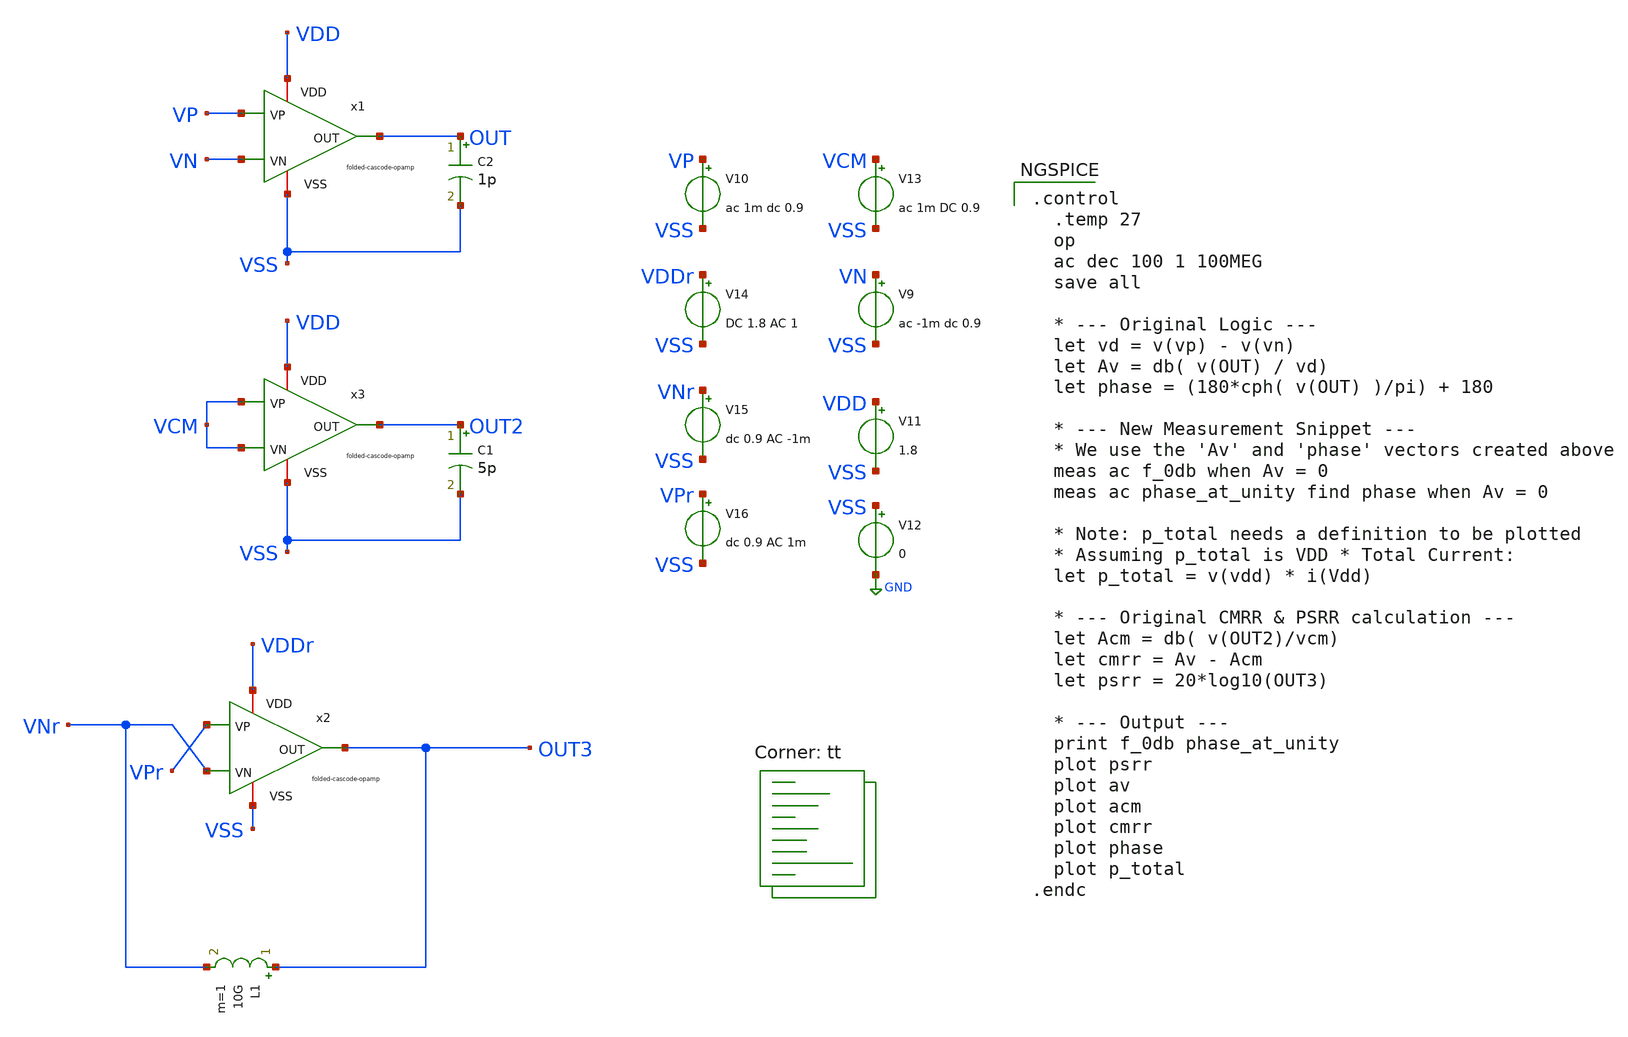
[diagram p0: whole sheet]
** sch_path: bandgap/bgr-opamp2/tb_ac.sch
**.subckt tb_ac
C2 OUT VSS 1p m=1
C1 OUT2 VSS 5p m=1
L1 OUT3 VNr 10G m=1
V9 VN VSS ac -1m dc 0.9
V10 VP VSS ac 1m dc 0.9
V11 VDD VSS 1.8
V12 VSS GND 0
V13 VCM VSS ac 1m DC 0.9
V14 VDDr VSS DC 1.8 AC 1
V15 VNr VSS dc 0.9 AC -1m
V16 VPr VSS dc 0.9 AC 1m
x1 OUT VDD VP VN VSS folded-cascode-opamp
x2 OUT3 VDDr VPr VNr VSS folded-cascode-opamp
x3 OUT2 VDD VCM VCM VSS folded-cascode-opamp
**** begin user architecture code

.control
  .temp 27
  op
  ac dec 100 1 100MEG
  save all

  * --- Original Logic ---
  let vd = v(vp) - v(vn)
  let Av = db( v(OUT) / vd)
  let phase = (180*cph( v(OUT) )/pi) + 180

  * --- New Measurement Snippet ---
  * We use the 'Av' and 'phase' vectors created above
  meas ac f_0db when Av = 0
  meas ac phase_at_unity find phase when Av = 0

  * Note: p_total needs a definition to be plotted
  * Assuming p_total is VDD * Total Current:
  let p_total = v(vdd) * i(Vdd)

  * --- Original CMRR & PSRR calculation ---
  let Acm = db( v(OUT2)/vcm)
  let cmrr = Av - Acm
  let psrr = 20*log10(OUT3)

  * --- Output ---
  print f_0db phase_at_unity
  plot psrr
  plot av
  plot acm
  plot cmrr
  plot phase
  plot p_total
.endc



.lib $::SKYWATER_MODELS/sky130.lib.spice tt
**** end user architecture code
**.ends

* expanding   symbol:  afe-icdec-teknofest-2026/bandgap/bgr-opamp2/folded-cascode-opamp.sym # of
*+ pins=5
** sym_path: bandgap/bgr-opamp2/folded-cascode-opamp.sym
** sch_path: bandgap/bgr-opamp2/folded-cascode-opamp.sch
.subckt folded-cascode-opamp OUT VDD VP VN VSS
*.iopin VSS
*.iopin VDD
*.ipin VP
*.ipin VN
*.opin OUT
XR10 VSS net8 VSS sky130_fd_pr__res_high_po_1p41 L=1.235 mult=1 m=1
XM19 net2 net2 VSS GND sky130_fd_pr__nfet_01v8_lvt L=0.5 W=6.4 nf=1 ad='int((nf+1)/2) * W/nf * 0.29'
+ as='int((nf+2)/2) * W/nf * 0.29' pd='2*int((nf+1)/2) * (W/nf + 0.29)' ps='2*int((nf+2)/2) * (W/nf + 0.29)'
+ nrd='0.29 / W' nrs='0.29 / W' sa=0 sb=0 sd=0 mult=1 m=1
XM20 net3 net2 net9 GND sky130_fd_pr__nfet_01v8_lvt L=0.5 W=6.4 nf=1 ad='int((nf+1)/2) * W/nf * 0.29'
+ as='int((nf+2)/2) * W/nf * 0.29' pd='2*int((nf+1)/2) * (W/nf + 0.29)' ps='2*int((nf+2)/2) * (W/nf + 0.29)'
+ nrd='0.29 / W' nrs='0.29 / W' sa=0 sb=0 sd=0 mult=1 m=1
XM16 net4 net1 VDD VDD sky130_fd_pr__pfet_01v8_lvt L=0.5 W=20.8 nf=1 ad='int((nf+1)/2) * W/nf * 0.29'
+ as='int((nf+2)/2) * W/nf * 0.29' pd='2*int((nf+1)/2) * (W/nf + 0.29)' ps='2*int((nf+2)/2) * (W/nf + 0.29)'
+ nrd='0.29 / W' nrs='0.29 / W' sa=0 sb=0 sd=0 mult=1 m=1
XM13 net1 net1 VDD VDD sky130_fd_pr__pfet_01v8_lvt L=0.5 W=20.8 nf=1 ad='int((nf+1)/2) * W/nf * 0.29'
+ as='int((nf+2)/2) * W/nf * 0.29' pd='2*int((nf+1)/2) * (W/nf + 0.29)' ps='2*int((nf+2)/2) * (W/nf + 0.29)'
+ nrd='0.29 / W' nrs='0.29 / W' sa=0 sb=0 sd=0 mult=1 m=1
XM14 net2 net3 net4 VDD sky130_fd_pr__pfet_01v8_lvt L=0.5 W=20.8 nf=1 ad='int((nf+1)/2) * W/nf * 0.29'
+ as='int((nf+2)/2) * W/nf * 0.29' pd='2*int((nf+1)/2) * (W/nf + 0.29)' ps='2*int((nf+2)/2) * (W/nf + 0.29)'
+ nrd='0.29 / W' nrs='0.29 / W' sa=0 sb=0 sd=0 mult=1 m=1
XM17 net3 net3 net1 VDD sky130_fd_pr__pfet_01v8_lvt L=0.5 W=20.8 nf=1 ad='int((nf+1)/2) * W/nf * 0.29'
+ as='int((nf+2)/2) * W/nf * 0.29' pd='2*int((nf+1)/2) * (W/nf + 0.29)' ps='2*int((nf+2)/2) * (W/nf + 0.29)'
+ nrd='0.29 / W' nrs='0.29 / W' sa=0 sb=0 sd=0 mult=1 m=1
XM18 net10 net1 VDD VDD sky130_fd_pr__pfet_01v8_lvt L=0.5 W=20.8 nf=1 ad='int((nf+1)/2) * W/nf * 0.29'
+ as='int((nf+2)/2) * W/nf * 0.29' pd='2*int((nf+1)/2) * (W/nf + 0.29)' ps='2*int((nf+2)/2) * (W/nf + 0.29)'
+ nrd='0.29 / W' nrs='0.29 / W' sa=0 sb=0 sd=0 mult=1 m=1
XM21 net11 net3 net10 VDD sky130_fd_pr__pfet_01v8_lvt L=0.5 W=20.8 nf=1 ad='int((nf+1)/2) * W/nf * 0.29'
+ as='int((nf+2)/2) * W/nf * 0.29' pd='2*int((nf+1)/2) * (W/nf + 0.29)' ps='2*int((nf+2)/2) * (W/nf + 0.29)'
+ nrd='0.29 / W' nrs='0.29 / W' sa=0 sb=0 sd=0 mult=1 m=1
XM22 net11 net11 net13 GND sky130_fd_pr__nfet_01v8_lvt L=0.5 W=1.45 nf=1 ad='int((nf+1)/2) * W/nf * 0.29'
+ as='int((nf+2)/2) * W/nf * 0.29' pd='2*int((nf+1)/2) * (W/nf + 0.29)' ps='2*int((nf+2)/2) * (W/nf + 0.29)'
+ nrd='0.29 / W' nrs='0.29 / W' sa=0 sb=0 sd=0 mult=1 m=1
XM23 net13 net11 net12 GND sky130_fd_pr__nfet_01v8_lvt L=0.5 W=1.45 nf=1 ad='int((nf+1)/2) * W/nf * 0.29'
+ as='int((nf+2)/2) * W/nf * 0.29' pd='2*int((nf+1)/2) * (W/nf + 0.29)' ps='2*int((nf+2)/2) * (W/nf + 0.29)'
+ nrd='0.29 / W' nrs='0.29 / W' sa=0 sb=0 sd=0 mult=1 m=1
XM24 net12 net11 VSS GND sky130_fd_pr__nfet_01v8_lvt L=0.5 W=1.45 nf=1 ad='int((nf+1)/2) * W/nf * 0.29'
+ as='int((nf+2)/2) * W/nf * 0.29' pd='2*int((nf+1)/2) * (W/nf + 0.29)' ps='2*int((nf+2)/2) * (W/nf + 0.29)'
+ nrd='0.29 / W' nrs='0.29 / W' sa=0 sb=0 sd=0 mult=1 m=1
XM26 net19 VN net14 VDD sky130_fd_pr__pfet_01v8_lvt L=1.25 W=64 nf=1 ad='int((nf+1)/2) * W/nf * 0.29'
+ as='int((nf+2)/2) * W/nf * 0.29' pd='2*int((nf+1)/2) * (W/nf + 0.29)' ps='2*int((nf+2)/2) * (W/nf + 0.29)'
+ nrd='0.29 / W' nrs='0.29 / W' sa=0 sb=0 sd=0 mult=1 m=1
XM27 net18 VP net14 VDD sky130_fd_pr__pfet_01v8_lvt L=1.25 W=64 nf=1 ad='int((nf+1)/2) * W/nf * 0.29'
+ as='int((nf+2)/2) * W/nf * 0.29' pd='2*int((nf+1)/2) * (W/nf + 0.29)' ps='2*int((nf+2)/2) * (W/nf + 0.29)'
+ nrd='0.29 / W' nrs='0.29 / W' sa=0 sb=0 sd=0 mult=1 m=1
XM15 net14 net20 VDD VDD sky130_fd_pr__pfet_01v8_lvt L=1.25 W=10.8 nf=1 ad='int((nf+1)/2) * W/nf * 0.29'
+ as='int((nf+2)/2) * W/nf * 0.29' pd='2*int((nf+1)/2) * (W/nf + 0.29)' ps='2*int((nf+2)/2) * (W/nf + 0.29)'
+ nrd='0.29 / W' nrs='0.29 / W' sa=0 sb=0 sd=0 mult=1 m=1
XM25 net16 net1 VDD VDD sky130_fd_pr__pfet_01v8_lvt L=1.25 W=10.4 nf=1 ad='int((nf+1)/2) * W/nf * 0.29'
+ as='int((nf+2)/2) * W/nf * 0.29' pd='2*int((nf+1)/2) * (W/nf + 0.29)' ps='2*int((nf+2)/2) * (W/nf + 0.29)'
+ nrd='0.29 / W' nrs='0.29 / W' sa=0 sb=0 sd=0 mult=1 m=1
XM28 net17 net1 VDD VDD sky130_fd_pr__pfet_01v8_lvt L=1.25 W=10.4 nf=1 ad='int((nf+1)/2) * W/nf * 0.29'
+ as='int((nf+2)/2) * W/nf * 0.29' pd='2*int((nf+1)/2) * (W/nf + 0.29)' ps='2*int((nf+2)/2) * (W/nf + 0.29)'
+ nrd='0.29 / W' nrs='0.29 / W' sa=0 sb=0 sd=0 mult=1 m=1
XM29 OUT net3 net16 VDD sky130_fd_pr__pfet_01v8_lvt L=1.25 W=10.4 nf=1 ad='int((nf+1)/2) * W/nf * 0.29'
+ as='int((nf+2)/2) * W/nf * 0.29' pd='2*int((nf+1)/2) * (W/nf + 0.29)' ps='2*int((nf+2)/2) * (W/nf + 0.29)'
+ nrd='0.29 / W' nrs='0.29 / W' sa=0 sb=0 sd=0 mult=1 m=1
XM30 net15 net3 net17 VDD sky130_fd_pr__pfet_01v8_lvt L=1.25 W=10.4 nf=1 ad='int((nf+1)/2) * W/nf * 0.29'
+ as='int((nf+2)/2) * W/nf * 0.29' pd='2*int((nf+1)/2) * (W/nf + 0.29)' ps='2*int((nf+2)/2) * (W/nf + 0.29)'
+ nrd='0.29 / W' nrs='0.29 / W' sa=0 sb=0 sd=0 mult=1 m=1
XM31 OUT net11 net19 GND sky130_fd_pr__nfet_01v8_lvt L=1.25 W=3.4 nf=1 ad='int((nf+1)/2) * W/nf * 0.29'
+ as='int((nf+2)/2) * W/nf * 0.29' pd='2*int((nf+1)/2) * (W/nf + 0.29)' ps='2*int((nf+2)/2) * (W/nf + 0.29)'
+ nrd='0.29 / W' nrs='0.29 / W' sa=0 sb=0 sd=0 mult=1 m=1
XM32 net15 net11 net18 GND sky130_fd_pr__nfet_01v8_lvt L=1.25 W=3.4 nf=1 ad='int((nf+1)/2) * W/nf * 0.29'
+ as='int((nf+2)/2) * W/nf * 0.29' pd='2*int((nf+1)/2) * (W/nf + 0.29)' ps='2*int((nf+2)/2) * (W/nf + 0.29)'
+ nrd='0.29 / W' nrs='0.29 / W' sa=0 sb=0 sd=0 mult=1 m=1
XM33 net19 net15 VSS GND sky130_fd_pr__nfet_01v8_lvt L=1.25 W=3.4 nf=1 ad='int((nf+1)/2) * W/nf * 0.29'
+ as='int((nf+2)/2) * W/nf * 0.29' pd='2*int((nf+1)/2) * (W/nf + 0.29)' ps='2*int((nf+2)/2) * (W/nf + 0.29)'
+ nrd='0.29 / W' nrs='0.29 / W' sa=0 sb=0 sd=0 mult=1 m=1
XM34 net18 net15 VSS GND sky130_fd_pr__nfet_01v8_lvt L=1.25 W=3.4 nf=1 ad='int((nf+1)/2) * W/nf * 0.29'
+ as='int((nf+2)/2) * W/nf * 0.29' pd='2*int((nf+1)/2) * (W/nf + 0.29)' ps='2*int((nf+2)/2) * (W/nf + 0.29)'
+ nrd='0.29 / W' nrs='0.29 / W' sa=0 sb=0 sd=0 mult=1 m=1
XM35 net20 net20 VDD VDD sky130_fd_pr__pfet_01v8_lvt L=1.25 W=10.8 nf=1 ad='int((nf+1)/2) * W/nf * 0.29'
+ as='int((nf+2)/2) * W/nf * 0.29' pd='2*int((nf+1)/2) * (W/nf + 0.29)' ps='2*int((nf+2)/2) * (W/nf + 0.29)'
+ nrd='0.29 / W' nrs='0.29 / W' sa=0 sb=0 sd=0 mult=1 m=1
XR6 VSS net23 VSS sky130_fd_pr__res_high_po_1p41 L=500 mult=1 m=1
XR1 net23 net21 VSS sky130_fd_pr__res_high_po_1p41 L=500 mult=1 m=1
XR2 net21 net22 VSS sky130_fd_pr__res_high_po_1p41 L=500 mult=1 m=1
XR3 net22 net24 VSS sky130_fd_pr__res_high_po_1p41 L=500 mult=1 m=1
XR4 net24 net20 VSS sky130_fd_pr__res_high_po_1p41 L=500 mult=1 m=1
XR5 net8 net6 VSS sky130_fd_pr__res_high_po_1p41 L=1.235 mult=1 m=1
XR7 net6 net7 VSS sky130_fd_pr__res_high_po_1p41 L=1.235 mult=1 m=1
XR8 net7 net5 VSS sky130_fd_pr__res_high_po_1p41 L=1.235 mult=1 m=1
XR9 net5 net9 VSS sky130_fd_pr__res_high_po_1p41 L=1.235 mult=1 m=1
.ends

.GLOBAL GND
.end
